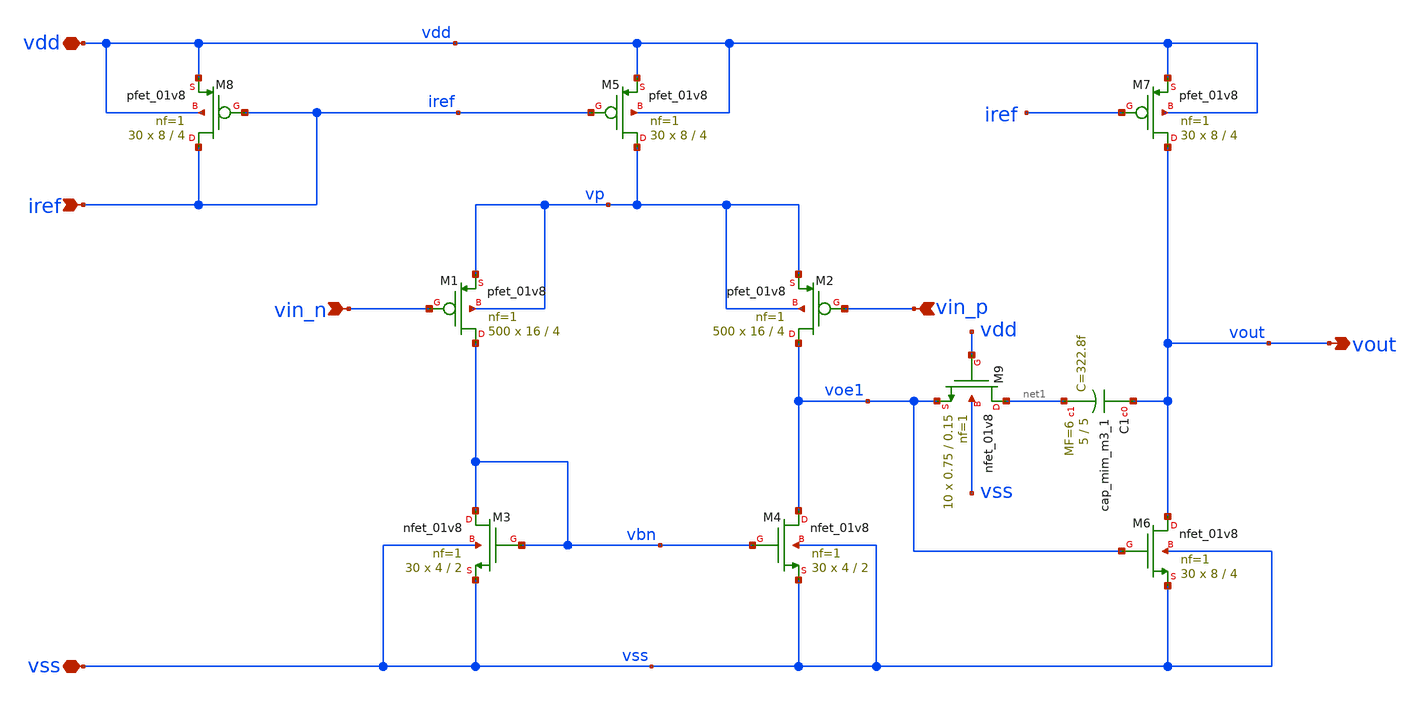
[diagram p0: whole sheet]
** sch_path: design/xschem/low_noise_amp_fc_v1.sch
**.subckt low_noise_amp_fc_v1 vdd vss vin_n vin_p iref vout
*.iopin vdd
*.iopin vss
*.ipin vin_n
*.ipin vin_p
*.ipin iref
*.opin vout
XM1 vbn vin_n vp vp sky130_fd_pr__pfet_01v8 L=4 W=16 nf=1 ad='W * 0.29' as='W * 0.29' pd='2 * (W + 0.29)'
+ ps='2 * (W + 0.29)' nrd='0.29 / W' nrs='0.29 / W' sa=0 sb=0 sd=0 mult=500 m=500
XM2 voe1 vin_p vp vp sky130_fd_pr__pfet_01v8 L=4 W=16 nf=1 ad='W * 0.29' as='W * 0.29' pd='2 * (W + 0.29)'
+ ps='2 * (W + 0.29)' nrd='0.29 / W' nrs='0.29 / W' sa=0 sb=0 sd=0 mult=500 m=500
XM3 vbn vbn vss vss sky130_fd_pr__nfet_01v8 L=2 W=4 nf=1 ad='W * 0.29' as='W * 0.29' pd='2 * (W + 0.29)'
+ ps='2 * (W + 0.29)' nrd='0.29 / W' nrs='0.29 / W' sa=0 sb=0 sd=0 mult=30 m=30
XM4 voe1 vbn vss vss sky130_fd_pr__nfet_01v8 L=2 W=4 nf=1 ad='W * 0.29' as='W * 0.29' pd='2 * (W + 0.29)'
+ ps='2 * (W + 0.29)' nrd='0.29 / W' nrs='0.29 / W' sa=0 sb=0 sd=0 mult=30 m=30
XM5 vp iref vdd vdd sky130_fd_pr__pfet_01v8 L=4 W=8 nf=1 ad='W * 0.29' as='W * 0.29' pd='2 * (W + 0.29)'
+ ps='2 * (W + 0.29)' nrd='0.29 / W' nrs='0.29 / W' sa=0 sb=0 sd=0 mult=30 m=30
XM7 vout iref vdd vdd sky130_fd_pr__pfet_01v8 L=4 W=8 nf=1 ad='W * 0.29' as='W * 0.29' pd='2 * (W + 0.29)'
+ ps='2 * (W + 0.29)' nrd='0.29 / W' nrs='0.29 / W' sa=0 sb=0 sd=0 mult=30 m=30
XM8 iref iref vdd vdd sky130_fd_pr__pfet_01v8 L=4 W=8 nf=1 ad='W * 0.29' as='W * 0.29' pd='2 * (W + 0.29)'
+ ps='2 * (W + 0.29)' nrd='0.29 / W' nrs='0.29 / W' sa=0 sb=0 sd=0 mult=30 m=30
XM6 vout voe1 vss vss sky130_fd_pr__nfet_01v8 L=4 W=8 nf=1 ad='W * 0.29' as='W * 0.29' pd='2 * (W + 0.29)'
+ ps='2 * (W + 0.29)' nrd='0.29 / W' nrs='0.29 / W' sa=0 sb=0 sd=0 mult=30 m=30
XM9 net1 vdd voe1 vss sky130_fd_pr__nfet_01v8 L=0.15 W=0.75 nf=1 ad='W * 0.29' as='W * 0.29' pd='2 * (W + 0.29)'
+ ps='2 * (W + 0.29)' nrd='0.29 / W' nrs='0.29 / W' sa=0 sb=0 sd=0 mult=10 m=10
XC1 vout net1 sky130_fd_pr__cap_mim_m3_1 W=5 L=5 MF=6 m=6
**.ends
.end
